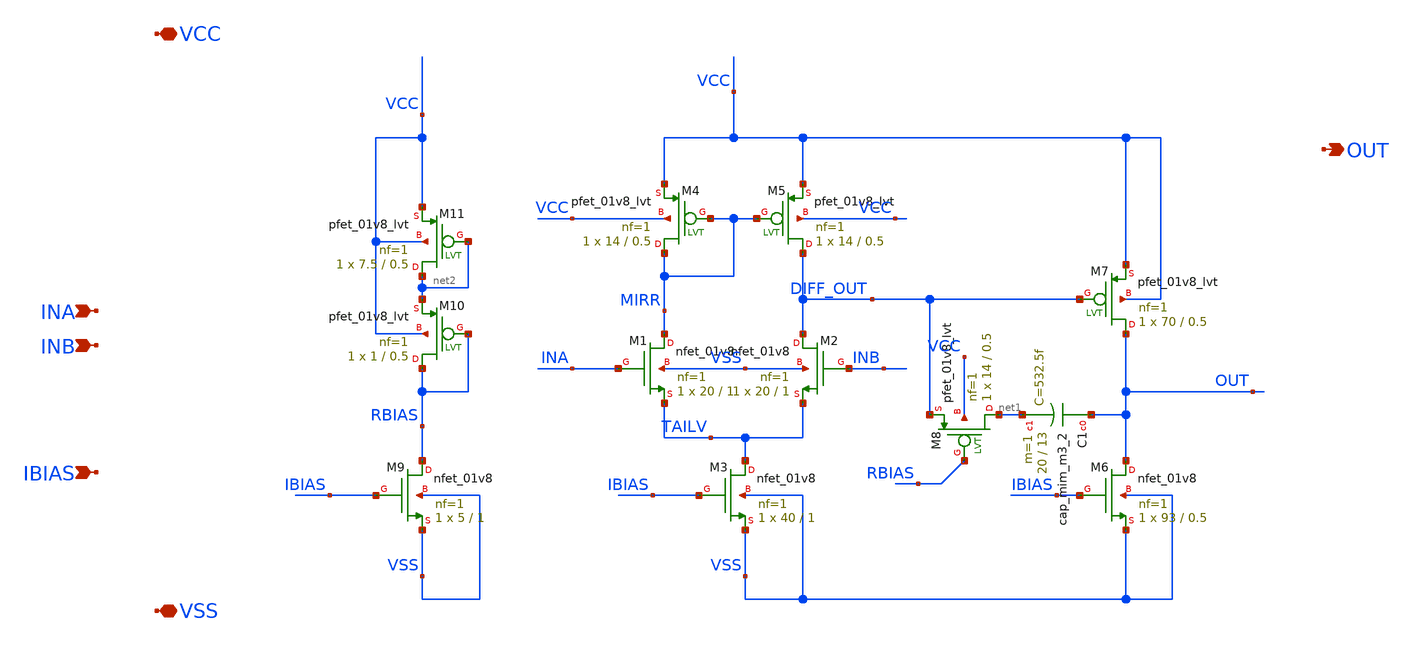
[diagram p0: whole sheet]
** sch_path: xschem/opamp_1.sch
**.subckt opamp_1 INA INB OUT VCC VSS IBIAS
*.ipin INA
*.ipin INB
*.opin OUT
*.iopin VCC
*.iopin VSS
*.ipin IBIAS
XM1 MIRR INA TAILV VSS sky130_fd_pr__nfet_01v8 L=1 W=20 nf=1 ad='int((nf+1)/2) * W/nf * 0.29' as='int((nf+2)/2) * W/nf * 0.29'
+ pd='2*int((nf+1)/2) * (W/nf + 0.29)' ps='2*int((nf+2)/2) * (W/nf + 0.29)' nrd='0.29 / W' nrs='0.29 / W'
+ sa=0 sb=0 sd=0 mult=1 m=1
XM2 DIFF_OUT INB TAILV VSS sky130_fd_pr__nfet_01v8 L=1 W=20 nf=1 ad='int((nf+1)/2) * W/nf * 0.29' as='int((nf+2)/2) * W/nf * 0.29'
+ pd='2*int((nf+1)/2) * (W/nf + 0.29)' ps='2*int((nf+2)/2) * (W/nf + 0.29)' nrd='0.29 / W' nrs='0.29 / W'
+ sa=0 sb=0 sd=0 mult=1 m=1
XM3 TAILV IBIAS VSS VSS sky130_fd_pr__nfet_01v8 L=1 W=40 nf=1 ad='int((nf+1)/2) * W/nf * 0.29' as='int((nf+2)/2) * W/nf * 0.29'
+ pd='2*int((nf+1)/2) * (W/nf + 0.29)' ps='2*int((nf+2)/2) * (W/nf + 0.29)' nrd='0.29 / W' nrs='0.29 / W'
+ sa=0 sb=0 sd=0 mult=1 m=1
XM4 MIRR MIRR VCC VCC sky130_fd_pr__pfet_01v8_lvt L=0.5 W=14 nf=1 ad='int((nf+1)/2) * W/nf * 0.29' as='int((nf+2)/2) * W/nf * 0.29'
+ pd='2*int((nf+1)/2) * (W/nf + 0.29)' ps='2*int((nf+2)/2) * (W/nf + 0.29)' nrd='0.29 / W' nrs='0.29 / W'
+ sa=0 sb=0 sd=0 mult=1 m=1
XM5 DIFF_OUT MIRR VCC VCC sky130_fd_pr__pfet_01v8_lvt L=0.5 W=14 nf=1 ad='int((nf+1)/2) * W/nf * 0.29'
+ as='int((nf+2)/2) * W/nf * 0.29' pd='2*int((nf+1)/2) * (W/nf + 0.29)' ps='2*int((nf+2)/2) * (W/nf + 0.29)'
+ nrd='0.29 / W' nrs='0.29 / W' sa=0 sb=0 sd=0 mult=1 m=1
XM6 OUT IBIAS VSS VSS sky130_fd_pr__nfet_01v8 L=0.5 W=93 nf=1 ad='int((nf+1)/2) * W/nf * 0.29' as='int((nf+2)/2) * W/nf * 0.29'
+ pd='2*int((nf+1)/2) * (W/nf + 0.29)' ps='2*int((nf+2)/2) * (W/nf + 0.29)' nrd='0.29 / W' nrs='0.29 / W'
+ sa=0 sb=0 sd=0 mult=1 m=1
XM7 OUT DIFF_OUT VCC VCC sky130_fd_pr__pfet_01v8_lvt L=0.5 W=70 nf=1 ad='int((nf+1)/2) * W/nf * 0.29'
+ as='int((nf+2)/2) * W/nf * 0.29' pd='2*int((nf+1)/2) * (W/nf + 0.29)' ps='2*int((nf+2)/2) * (W/nf + 0.29)'
+ nrd='0.29 / W' nrs='0.29 / W' sa=0 sb=0 sd=0 mult=1 m=1
XM9 RBIAS IBIAS VSS VSS sky130_fd_pr__nfet_01v8 L=1 W=5 nf=1 ad='int((nf+1)/2) * W/nf * 0.29' as='int((nf+2)/2) * W/nf * 0.29'
+ pd='2*int((nf+1)/2) * (W/nf + 0.29)' ps='2*int((nf+2)/2) * (W/nf + 0.29)' nrd='0.29 / W' nrs='0.29 / W'
+ sa=0 sb=0 sd=0 mult=1 m=1
XM10 RBIAS RBIAS net2 VCC sky130_fd_pr__pfet_01v8_lvt L=0.5 W=1 nf=1 ad='int((nf+1)/2) * W/nf * 0.29'
+ as='int((nf+2)/2) * W/nf * 0.29' pd='2*int((nf+1)/2) * (W/nf + 0.29)' ps='2*int((nf+2)/2) * (W/nf + 0.29)'
+ nrd='0.29 / W' nrs='0.29 / W' sa=0 sb=0 sd=0 mult=1 m=1
XM11 net2 net2 VCC VCC sky130_fd_pr__pfet_01v8_lvt L=0.5 W=7.5 nf=1 ad='int((nf+1)/2) * W/nf * 0.29'
+ as='int((nf+2)/2) * W/nf * 0.29' pd='2*int((nf+1)/2) * (W/nf + 0.29)' ps='2*int((nf+2)/2) * (W/nf + 0.29)'
+ nrd='0.29 / W' nrs='0.29 / W' sa=0 sb=0 sd=0 mult=1 m=1
XC1 OUT net1 sky130_fd_pr__cap_mim_m3_2 W=20 L=13 MF=1 m=1
XM8 net1 RBIAS DIFF_OUT VCC sky130_fd_pr__pfet_01v8_lvt L=0.5 W=14 nf=1 ad='int((nf+1)/2) * W/nf * 0.29'
+ as='int((nf+2)/2) * W/nf * 0.29' pd='2*int((nf+1)/2) * (W/nf + 0.29)' ps='2*int((nf+2)/2) * (W/nf + 0.29)'
+ nrd='0.29 / W' nrs='0.29 / W' sa=0 sb=0 sd=0 mult=1 m=1
**.ends
.end
